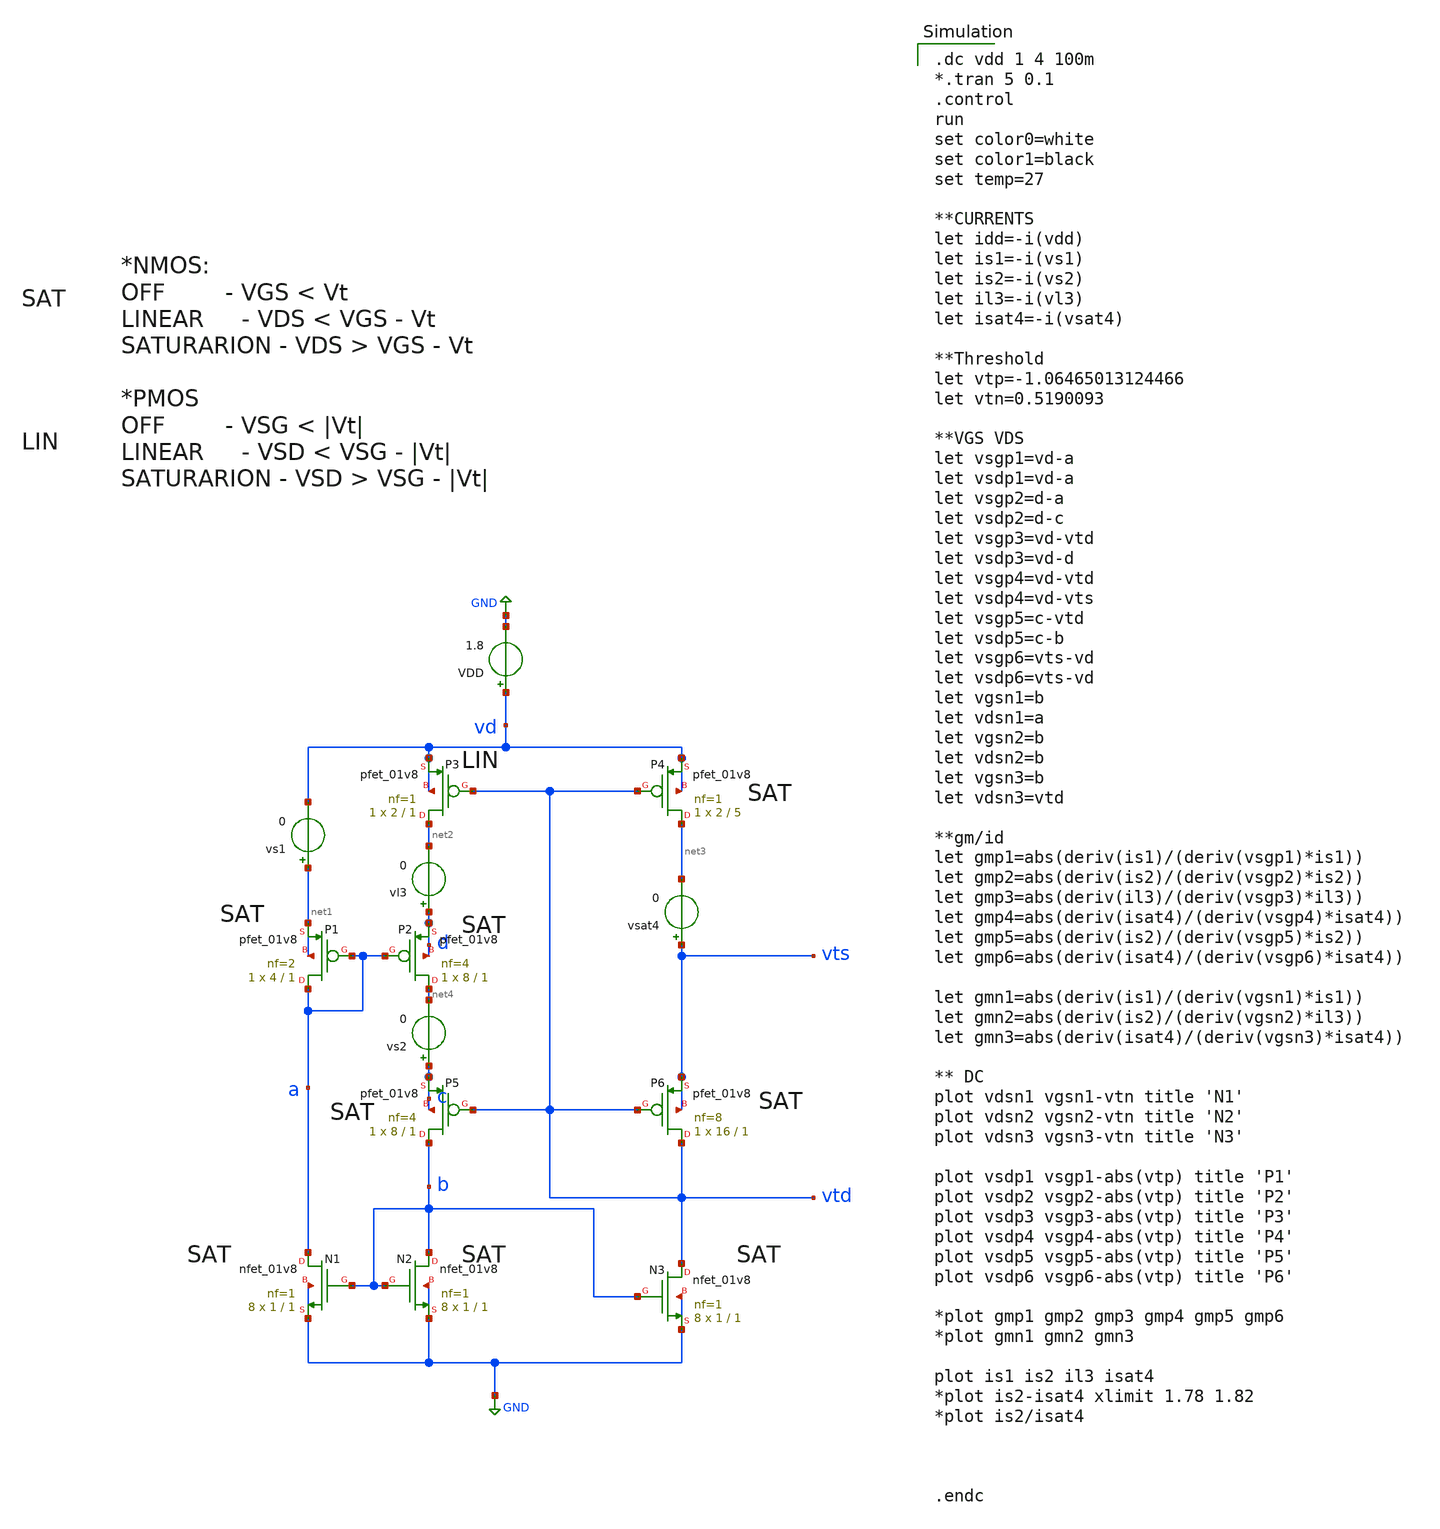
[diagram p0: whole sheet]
** sch_path: sensor/xschem/temp-tb-dc.sch
**.subckt temp-tb-dc
VDD vd GND 1.8
vs1 net1 vd 0
vs2 c net4 0
vl3 d net2 0
vsat4 vts net3 0
XP1 a a net1 net1 sky130_fd_pr__pfet_01v8 L=1 W=4 nf=2 ad='int((nf+1)/2) * W/nf * 0.29' as='int((nf+2)/2) * W/nf * 0.29'
+ pd='2*int((nf+1)/2) * (W/nf + 0.29)' ps='2*int((nf+2)/2) * (W/nf + 0.29)' nrd='0.29 / W' nrs='0.29 / W'
+ sa=0 sb=0 sd=0 mult=1 m=1
XP2 net4 a d d sky130_fd_pr__pfet_01v8 L=1 W=8 nf=4 ad='int((nf+1)/2) * W/nf * 0.29' as='int((nf+2)/2) * W/nf * 0.29'
+ pd='2*int((nf+1)/2) * (W/nf + 0.29)' ps='2*int((nf+2)/2) * (W/nf + 0.29)' nrd='0.29 / W' nrs='0.29 / W'
+ sa=0 sb=0 sd=0 mult=1 m=1
XP3 net2 vtd vd vd sky130_fd_pr__pfet_01v8 L=1 W=2 nf=1 ad='int((nf+1)/2) * W/nf * 0.29' as='int((nf+2)/2) * W/nf * 0.29'
+ pd='2*int((nf+1)/2) * (W/nf + 0.29)' ps='2*int((nf+2)/2) * (W/nf + 0.29)' nrd='0.29 / W' nrs='0.29 / W'
+ sa=0 sb=0 sd=0 mult=1 m=1
XP4 net3 vtd vd vd sky130_fd_pr__pfet_01v8 L=5 W=2 nf=1 ad='int((nf+1)/2) * W/nf * 0.29' as='int((nf+2)/2) * W/nf * 0.29'
+ pd='2*int((nf+1)/2) * (W/nf + 0.29)' ps='2*int((nf+2)/2) * (W/nf + 0.29)' nrd='0.29 / W' nrs='0.29 / W'
+ sa=0 sb=0 sd=0 mult=1 m=1
XP5 b vtd c c sky130_fd_pr__pfet_01v8 L=1 W=8 nf=4 ad='int((nf+1)/2) * W/nf * 0.29' as='int((nf+2)/2) * W/nf * 0.29'
+ pd='2*int((nf+1)/2) * (W/nf + 0.29)' ps='2*int((nf+2)/2) * (W/nf + 0.29)' nrd='0.29 / W' nrs='0.29 / W'
+ sa=0 sb=0 sd=0 mult=1 m=1
XP6 vtd vtd vts vts sky130_fd_pr__pfet_01v8 L=1 W=16 nf=8 ad='int((nf+1)/2) * W/nf * 0.29' as='int((nf+2)/2) * W/nf * 0.29'
+ pd='2*int((nf+1)/2) * (W/nf + 0.29)' ps='2*int((nf+2)/2) * (W/nf + 0.29)' nrd='0.29 / W' nrs='0.29 / W'
+ sa=0 sb=0 sd=0 mult=1 m=1
XN1 a b GND GND sky130_fd_pr__nfet_01v8 L=1 W=1 nf=1 ad='int((nf+1)/2) * W/nf * 0.29' as='int((nf+2)/2) * W/nf * 0.29'
+ pd='2*int((nf+1)/2) * (W/nf + 0.29)' ps='2*int((nf+2)/2) * (W/nf + 0.29)' nrd='0.29 / W' nrs='0.29 / W'
+ sa=0 sb=0 sd=0 mult=8 m=8
XN2 b b GND GND sky130_fd_pr__nfet_01v8 L=1 W=1 nf=1 ad='int((nf+1)/2) * W/nf * 0.29' as='int((nf+2)/2) * W/nf * 0.29'
+ pd='2*int((nf+1)/2) * (W/nf + 0.29)' ps='2*int((nf+2)/2) * (W/nf + 0.29)' nrd='0.29 / W' nrs='0.29 / W'
+ sa=0 sb=0 sd=0 mult=8 m=8
XN3 vtd b GND GND sky130_fd_pr__nfet_01v8 L=1 W=1 nf=1 ad='int((nf+1)/2) * W/nf * 0.29' as='int((nf+2)/2) * W/nf * 0.29'
+ pd='2*int((nf+1)/2) * (W/nf + 0.29)' ps='2*int((nf+2)/2) * (W/nf + 0.29)' nrd='0.29 / W' nrs='0.29 / W'
+ sa=0 sb=0 sd=0 mult=8 m=8
**** begin user architecture code

.dc vdd 1 4 100m
*.tran 5 0.1
.control
run
set color0=white
set color1=black
set temp=27

**CURRENTS
let idd=-i(vdd)
let is1=-i(vs1)
let is2=-i(vs2)
let il3=-i(vl3)
let isat4=-i(vsat4)

**Threshold
let vtp=-1.06465013124466
let vtn=0.5190093

**VGS VDS
let vsgp1=vd-a
let vsdp1=vd-a
let vsgp2=d-a
let vsdp2=d-c
let vsgp3=vd-vtd
let vsdp3=vd-d
let vsgp4=vd-vtd
let vsdp4=vd-vts
let vsgp5=c-vtd
let vsdp5=c-b
let vsgp6=vts-vd
let vsdp6=vts-vd
let vgsn1=b
let vdsn1=a
let vgsn2=b
let vdsn2=b
let vgsn3=b
let vdsn3=vtd

**gm/id
let gmp1=abs(deriv(is1)/(deriv(vsgp1)*is1))
let gmp2=abs(deriv(is2)/(deriv(vsgp2)*is2))
let gmp3=abs(deriv(il3)/(deriv(vsgp3)*il3))
let gmp4=abs(deriv(isat4)/(deriv(vsgp4)*isat4))
let gmp5=abs(deriv(is2)/(deriv(vsgp5)*is2))
let gmp6=abs(deriv(isat4)/(deriv(vsgp6)*isat4))

let gmn1=abs(deriv(is1)/(deriv(vgsn1)*is1))
let gmn2=abs(deriv(is2)/(deriv(vgsn2)*il3))
let gmn3=abs(deriv(isat4)/(deriv(vgsn3)*isat4))

** DC
plot vdsn1 vgsn1-vtn title 'N1'
plot vdsn2 vgsn2-vtn title 'N2'
plot vdsn3 vgsn3-vtn title 'N3'

plot vsdp1 vsgp1-abs(vtp) title 'P1'
plot vsdp2 vsgp2-abs(vtp) title 'P2'
plot vsdp3 vsgp3-abs(vtp) title 'P3'
plot vsdp4 vsgp4-abs(vtp) title 'P4'
plot vsdp5 vsgp5-abs(vtp) title 'P5'
plot vsdp6 vsgp6-abs(vtp) title 'P6'

*plot gmp1 gmp2 gmp3 gmp4 gmp5 gmp6
*plot gmn1 gmn2 gmn3

plot is1 is2 il3 isat4
*plot is2-isat4 xlimit 1.78 1.82
*plot is2/isat4



.endc



.lib /home/hugodg/sky130_workspace/skywater-pdk/libraries/sky130_fd_pr_ngspice/latest/models/sky130.lib.spice tt



R0 vd.n23 vd.n22 222.87
R1 vd.n10 vd.n9 222.87
R2 vd.n24 vd.n23 149.458
R3 vd.n11 vd.n10 149.458
R4 vd.n26 vd.n12 0.85
R5 vd.n26 vd.n25 0.375
R6 vd.n25 vd.n15 0.37
R7 vd.n12 vd.n2 0.37
R8 vd vd.n26 0.112
R9 vd.n25 vd.n24 0.017
R10 vd.n12 vd.n11 0.017
R11 vd.n22 vd.n21 0.015
R12 vd.n9 vd.n8 0.015
R13 vd.n23 vd.n20 0.008
R14 vd.n17 vd.n16 0.008
R15 vd.n10 vd.n7 0.008
R16 vd.n4 vd.n3 0.008
R17 vd.n20 vd.n19 0.006
R18 vd.n7 vd.n6 0.006
R19 vd.n18 vd.n17 0.006
R20 vd.n5 vd.n4 0.006
R21 vd.n19 vd.n18 0.004
R22 vd.n6 vd.n5 0.004
R23 vd.n15 vd.n14 0.001
R24 vd.n2 vd.n1 0.001
R25 vd.n14 vd.n13 0.001
R26 vd.n1 vd.n0 0.001
R27 vtd.n19 vtd.t21 64.503
R28 vtd.n1 vtd.t20 63.858
R29 vtd.n11 vtd.t0 63.734
R30 vtd.n17 vtd.t18 63.628
R31 vtd.n16 vtd.t17 63.628
R32 vtd.n15 vtd.t2 63.628
R33 vtd.n13 vtd.t4 63.628
R34 vtd.n12 vtd.t6 63.628
R35 vtd.n8 vtd.t8 63.628
R36 vtd.n4 vtd.t12 63.628
R37 vtd.n5 vtd.t14 63.628
R38 vtd.n1 vtd.t19 63.628
R39 vtd.n2 vtd.t10 63.628
R40 vtd.n10 vtd.t1 14.282
R41 vtd.n10 vtd.t7 14.282
R42 vtd.n9 vtd.t5 14.282
R43 vtd.n9 vtd.t3 14.282
R44 vtd.n6 vtd.t9 14.282
R45 vtd.n6 vtd.t15 14.282
R46 vtd.n0 vtd.t13 14.282
R47 vtd.n0 vtd.t11 14.282
R48 vtd.n19 vtd.t16 12.724
R49 vtd.n2 vtd.n1 0.787
R50 vtd.n16 vtd.n15 0.769
R51 vtd vtd.n20 0.568
R52 vtd.n18 vtd.n17 0.478
R53 vtd.n20 vtd.n18 0.244
R54 vtd.n17 vtd.n16 0.23
R55 vtd.n20 vtd.n19 0.16
R56 vtd.n8 vtd.n7 0.105
R57 vtd.n15 vtd.n14 0.1
R58 vtd.n3 vtd.n2 0.1
R59 vtd.n13 vtd.n12 0.089
R60 vtd.n5 vtd.n4 0.089
R61 vtd.n18 vtd.n8 0.08
R62 vtd.n11 vtd.n10 0.061
R63 vtd.n7 vtd.n6 0.061
R64 vtd.n14 vtd.n9 0.057
R65 vtd.n3 vtd.n0 0.057
R66 vtd.n12 vtd.n11 0.045
R67 vtd.n7 vtd.n5 0.045
R68 vtd.n14 vtd.n13 0.044
R69 vtd.n4 vtd.n3 0.044
R70 vts.n6 vts.n5 151.046
R71 vts.n8 vts.n7 149.458
R72 vts vts.n9 2.772
R73 vts.n9 vts.n6 1.514
R74 vts.n9 vts.n8 0.017
R75 vts.n5 vts.n4 0.008
R76 vts.n1 vts.n0 0.004
R77 vts.n2 vts.n1 0.004
R78 vts.n3 vts.n2 0.001
R79 vts.n6 vts.n3 0.001
R80 b.n1 b.t7 17.619
R81 b.n7 b.t4 18.027
R82 b.n0 b.t3 17.404
R83 b.n2 b.t2 17.404
R84 b.n2 b.t6 18.003
R85 b.n11 b.t0 17.404
R86 b.n9 b.t5 17.404
R87 b.n7 b.t1 17.404
R88 b.n19 b.n12 6.22
R89 b.n16 b.n15 4.5
R90 b.n16 b.n14 4.5
R91 b.n4 b.n1 3.868
R92 b.n4 b.n3 3.839
R93 b.n17 b.n16 2.625
R94 b.n6 b.n5 1.507
R95 b b.n19 0.928
R96 b.n6 b.n4 0.708
R97 b.n19 b.n6 0.708
R98 b.n18 b.n17 0.708
R99 b.n19 b.n18 0.666
R100 b.n9 b.n8 0.45
R101 b.n11 b.n10 0.448
R102 b.n1 b.n0 0.356
R103 b.n12 b.n11 0.17
R104 b.n10 b.n9 0.168
R105 b.n3 b.n2 0.16
R106 b.n8 b.n7 0.159
R107 b.n14 b.n13 0.113
R108 gnd.n0 gnd.n5 732.611
R109 gnd.n0 gnd.n3 732.611
R110 gnd.n34 gnd.n33 732.611
R111 gnd.n34 gnd.n10 732.611
R112 gnd.n44 gnd.n43 732.611
R113 gnd.n44 gnd.n40 732.611
R114 gnd.n10 gnd.n8 659.199
R115 gnd.n40 gnd.n38 659.199
R116 gnd.n33 gnd.n31 653.176
R117 gnd.n43 gnd.n41 649.411
R118 gnd.n30 gnd.n16 31.079
R119 gnd.n8 gnd.n7 30.494
R120 gnd.n16 gnd.n11 19.019
R121 gnd.n23 gnd.n22 9.3
R122 gnd.n16 gnd.n15 9.3
R123 gnd.n20 gnd.n19 9.3
R124 gnd.n38 gnd.n35 7.529
R125 gnd.n49 gnd.n48 7.152
R126 gnd.n31 gnd.n30 6.023
R127 gnd.n6 gnd.n57 2.258
R128 gnd.n0 gnd.n21 1.876
R129 gnd.n66 gnd.n65 0.186
R130 gnd.n64 gnd.n63 0.18
R131 gnd.n59 gnd.n58 0.107
R132 gnd.n27 gnd.n26 0.102
R133 gnd.n24 gnd.n20 0.077
R134 gnd.n15 gnd.n14 0.072
R135 gnd gnd.n1 0.07
R136 gnd.n66 gnd.n62 0.069
R137 gnd.n0 gnd.n23 0.067
R138 gnd.n28 gnd.n27 0.066
R139 gnd.n37 gnd.n36 0.062
R140 gnd.n25 gnd.n18 0.056
R141 gnd.n1 gnd.n70 0.055
R142 gnd.n60 gnd.n56 0.052
R143 gnd.n61 gnd.n60 0.046
R144 gnd.n1 gnd.n67 0.046
R145 gnd.n59 gnd.n6 0.046
R146 gnd.n24 gnd.n0 0.046
R147 gnd.n1 gnd.n34 0.046
R148 gnd.n6 gnd.n44 0.046
R149 gnd.n1 gnd.n69 0.045
R150 gnd.n29 gnd.n17 0.039
R151 gnd.n29 gnd.n28 0.039
R152 gnd.n67 gnd.n45 0.034
R153 gnd.n61 gnd.n51 0.034
R154 gnd.n15 gnd.n12 0.031
R155 gnd.n55 gnd.n53 0.03
R156 gnd.n30 gnd.n29 0.03
R157 gnd.n51 gnd.n50 0.025
R158 gnd.n14 gnd.n13 0.023
R159 gnd.n60 gnd.n59 0.019
R160 gnd.n50 gnd.n47 0.018
R161 gnd.n38 gnd.n37 0.017
R162 gnd.n50 gnd.n49 0.017
R163 gnd.n66 gnd.n64 0.012
R164 gnd.n53 gnd.n52 0.011
R165 gnd.n56 gnd.n55 0.01
R166 gnd.n26 gnd.n25 0.009
R167 gnd.n25 gnd.n24 0.006
R168 gnd.n69 gnd.n68 0.005
R169 gnd.n5 gnd.n4 0.004
R170 gnd.n3 gnd.n2 0.004
R171 gnd.n33 gnd.n32 0.004
R172 gnd.n10 gnd.n9 0.004
R173 gnd.n43 gnd.n42 0.004
R174 gnd.n40 gnd.n39 0.004
R175 gnd.n55 gnd.n54 0.002
R176 gnd.n67 gnd.n66 0.001
R177 gnd.n62 gnd.n61 0.001
R178 gnd.n62 gnd.n46 0.001
C0 vts vtd 7.80fF
C1 b c 2.09fF
C2 vd vtd 2.64fF
C3 vtd c 3.54fF
C4 vtd b 5.31fF
C5 a d 4.24fF
C6 a vts 0.90fF
C7 a vd 0.99fF
C8 a c 1.42fF
C9 a b 4.95fF
C10 d vts 0.21fF
C11 d vd 1.91fF
C12 a vtd 1.18fF
C13 d c 1.52fF
C14 d b 0.38fF
C15 d vtd 0.54fF
C16 vd vts 0.43fF
C17 vts c 1.96fF
C18 vts b 4.21fF
C19 vd c 0.64fF
C20 vd b 0.24fF
C21 b.t7 gnd 0.15fF
C22 b.t3 gnd 0.10fF
C23 b.n0 gnd 2.66fF $ **FLOATING
C24 b.n1 gnd 7.23fF $ **FLOATING
C25 b.t6 gnd 0.18fF
C26 b.t2 gnd 0.10fF
C27 b.n2 gnd 3.85fF $ **FLOATING
C28 b.n3 gnd 3.44fF $ **FLOATING
C29 b.n4 gnd 14.60fF $ **FLOATING
C30 b.n5 gnd 4.96fF $ **FLOATING
C31 b.n6 gnd 2.62fF $ **FLOATING
C32 b.t4 gnd 0.17fF
C33 b.t1 gnd 0.10fF
C34 b.n7 gnd 3.24fF $ **FLOATING
C35 b.n8 gnd 2.43fF $ **FLOATING
C36 b.t5 gnd 0.10fF
C37 b.n9 gnd 1.17fF $ **FLOATING
C38 b.n10 gnd 2.45fF $ **FLOATING
C39 b.t0 gnd 0.10fF
C40 b.n11 gnd 1.19fF $ **FLOATING
C41 b.n12 gnd 2.60fF $ **FLOATING
C42 b.n13 gnd 0.26fF $ **FLOATING
C43 b.n14 gnd 0.19fF $ **FLOATING
C44 b.n15 gnd 0.08fF $ **FLOATING
C45 b.n16 gnd 4.36fF $ **FLOATING
C46 b.n17 gnd 7.09fF $ **FLOATING
C47 b.n18 gnd 5.66fF $ **FLOATING
C48 b.n19 gnd 7.78fF $ **FLOATING
C49 vts.n0 gnd 0.19fF $ **FLOATING
C50 vts.n1 gnd 0.19fF $ **FLOATING
C51 vts.n3 gnd 3.30fF $ **FLOATING
C52 vts.n4 gnd 1.95fF $ **FLOATING
C53 vts.n5 gnd 0.14fF $ **FLOATING
C54 vts.n6 gnd 0.33fF $ **FLOATING
C55 vts.n7 gnd 2.08fF $ **FLOATING
C56 vts.n8 gnd 0.10fF $ **FLOATING
C57 vts.n9 gnd 8.26fF $ **FLOATING
C58 vtd.t8 gnd 0.47fF
C59 vtd.t14 gnd 0.47fF
C60 vtd.t12 gnd 0.47fF
C61 vtd.t13 gnd 0.03fF
C62 vtd.t11 gnd 0.03fF
C63 vtd.n0 gnd 0.13fF $ **FLOATING
C64 vtd.t10 gnd 0.47fF
C65 vtd.t19 gnd 0.47fF
C66 vtd.t20 gnd 0.47fF
C67 vtd.n1 gnd 0.89fF $ **FLOATING
C68 vtd.n2 gnd 0.51fF $ **FLOATING
C69 vtd.n3 gnd 0.18fF $ **FLOATING
C70 vtd.n4 gnd 0.51fF $ **FLOATING
C71 vtd.n5 gnd 0.51fF $ **FLOATING
C72 vtd.t9 gnd 0.03fF
C73 vtd.t15 gnd 0.03fF
C74 vtd.n6 gnd 0.13fF $ **FLOATING
C75 vtd.n7 gnd 0.18fF $ **FLOATING
C76 vtd.n8 gnd 0.25fF $ **FLOATING
C77 vtd.t5 gnd 0.03fF
C78 vtd.t3 gnd 0.03fF
C79 vtd.n9 gnd 0.13fF $ **FLOATING
C80 vtd.t0 gnd 0.47fF
C81 vtd.t1 gnd 0.03fF
C82 vtd.t7 gnd 0.03fF
C83 vtd.n10 gnd 0.13fF $ **FLOATING
C84 vtd.n11 gnd 0.46fF $ **FLOATING
C85 vtd.t6 gnd 0.47fF
C86 vtd.n12 gnd 0.51fF $ **FLOATING
C87 vtd.t4 gnd 0.47fF
C88 vtd.n13 gnd 0.51fF $ **FLOATING
C89 vtd.n14 gnd 0.18fF $ **FLOATING
C90 vtd.t2 gnd 0.47fF
C91 vtd.n15 gnd 0.50fF $ **FLOATING
C92 vtd.t17 gnd 0.47fF
C93 vtd.n16 gnd 0.55fF $ **FLOATING
C94 vtd.t18 gnd 0.47fF
C95 vtd.n17 gnd 0.44fF $ **FLOATING
C96 vtd.n18 gnd 0.54fF $ **FLOATING
C97 vtd.t16 gnd 2.35fF
C98 vtd.t21 gnd 0.48fF
C99 vtd.n19 gnd 2.32fF $ **FLOATING
C100 vtd.n20 gnd 7.12fF $ **FLOATING
C101 vd.n0 gnd 0.62fF $ **FLOATING
C102 vd.n1 gnd 0.03fF $ **FLOATING
C103 vd.n2 gnd 0.09fF $ **FLOATING
C104 vd.n3 gnd 0.07fF $ **FLOATING
C105 vd.n4 gnd 0.08fF $ **FLOATING
C106 vd.n5 gnd 0.42fF $ **FLOATING
C107 vd.n6 gnd 0.42fF $ **FLOATING
C108 vd.n7 gnd 0.08fF $ **FLOATING
C109 vd.n8 gnd 0.62fF $ **FLOATING
C110 vd.n9 gnd 0.08fF $ **FLOATING
C111 vd.n10 gnd 0.07fF $ **FLOATING
C112 vd.n11 gnd 0.04fF $ **FLOATING
C113 vd.n12 gnd 0.98fF $ **FLOATING
C114 vd.n13 gnd 0.62fF $ **FLOATING
C115 vd.n14 gnd 0.03fF $ **FLOATING
C116 vd.n15 gnd 0.09fF $ **FLOATING
C117 vd.n16 gnd 0.07fF $ **FLOATING
C118 vd.n17 gnd 0.08fF $ **FLOATING
C119 vd.n18 gnd 0.42fF $ **FLOATING
C120 vd.n19 gnd 0.42fF $ **FLOATING
C121 vd.n20 gnd 0.08fF $ **FLOATING
C122 vd.n21 gnd 0.62fF $ **FLOATING
C123 vd.n22 gnd 0.08fF $ **FLOATING
C124 vd.n23 gnd 0.07fF $ **FLOATING
C125 vd.n24 gnd 0.04fF $ **FLOATING
C126 vd.n25 gnd 14.58fF $ **FLOATING
C127 vd.n26 gnd 3.50fF $ **FLOATING
C128 d gnd 9.68fF
C129 a gnd 10.08fF
C130 c gnd -15.39fF
C131 b gnd 131.16fF
C132 vtd gnd -35.85fF
C133 vts gnd 18.71fF
C134 vd gnd 13.44fF


**** end user architecture code
**.ends
.GLOBAL GND
.end
